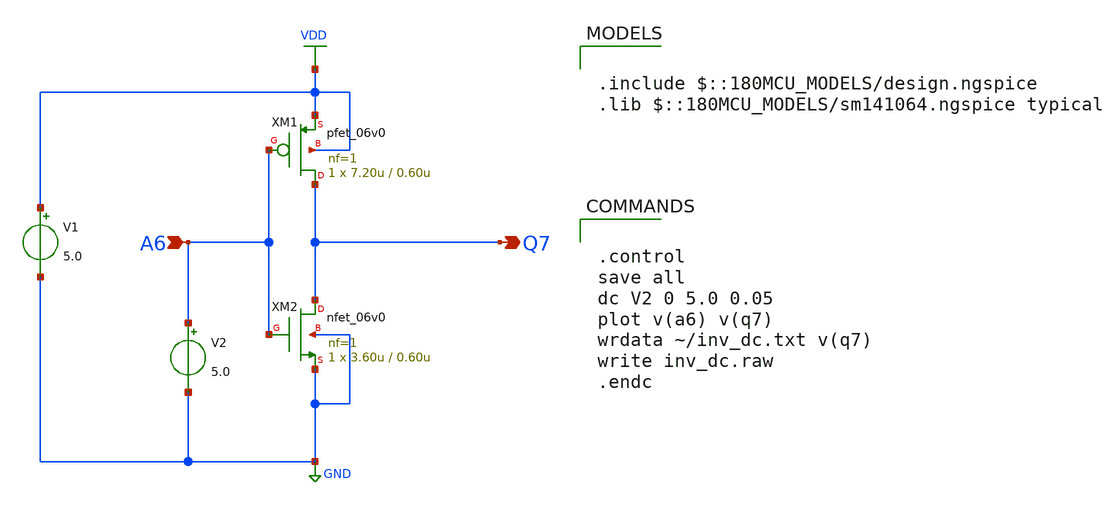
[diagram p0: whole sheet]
** sch_path: member_project/noritsuna/inverter/xschem/inverter_allin.sch
**.subckt inverter_allin A6 Q7
*.ipin A6
*.opin Q7
XM1 Q7 A6 VDD VDD pfet_06v0 L=0.60u W=7.20u nf=1 ad='int((nf+1)/2) * W/nf * 0.18u' as='int((nf+2)/2) * W/nf * 0.18u'
+ pd='2*int((nf+1)/2) * (W/nf + 0.18u)' ps='2*int((nf+2)/2) * (W/nf + 0.18u)' nrd='0.18u / W' nrs='0.18u / W'
+ sa=0 sb=0 sd=0 m=1
XM2 Q7 A6 GND GND nfet_06v0 L=0.60u W=3.60u nf=1 ad='int((nf+1)/2) * W/nf * 0.18u' as='int((nf+2)/2) * W/nf * 0.18u'
+ pd='2*int((nf+1)/2) * (W/nf + 0.18u)' ps='2*int((nf+2)/2) * (W/nf + 0.18u)' nrd='0.18u / W' nrs='0.18u / W'
+ sa=0 sb=0 sd=0 m=1
V1 VDD GND 5.0
V2 A6 GND 5.0
**** begin user architecture code

.include $::180MCU_MODELS/design.ngspice
.lib $::180MCU_MODELS/sm141064.ngspice typical



.control
save all
dc V2 0 5.0 0.05
plot v(a6) v(q7)
wrdata ~/inv_dc.txt v(q7)
write inv_dc.raw
.endc


**** end user architecture code
**.ends
.GLOBAL GND
.GLOBAL VDD
.end
